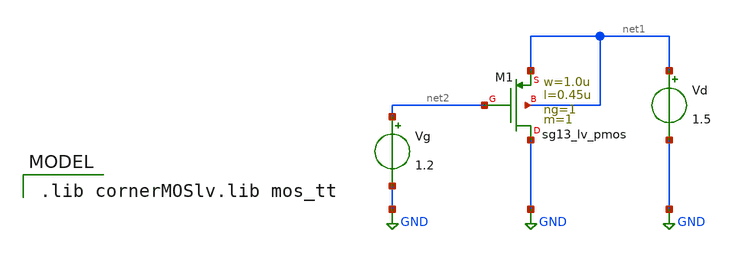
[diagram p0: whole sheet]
** sch_path: Taller1/Resuelto/Pmoslv_test.sch
**.subckt Pmoslv_test
Vg net2 GND 1.2
Vd net1 GND 1.5
XM1 GND net2 net1 net1 sg13_lv_pmos w=1.0u l=0.45u ng=1 m=1 mm_ok=1
**** begin user architecture code
 .lib cornerMOSlv.lib mos_tt




.control
save all
save @n.xm1.nsg13_lv_pmos[ids]
dc vg 0.0 1.5 0.01
let id = @n.xm1.nsg13_lv_pmos[ids]
plot id
plot log(id)
.endc


**** end user architecture code
**.ends
.GLOBAL GND
.end
